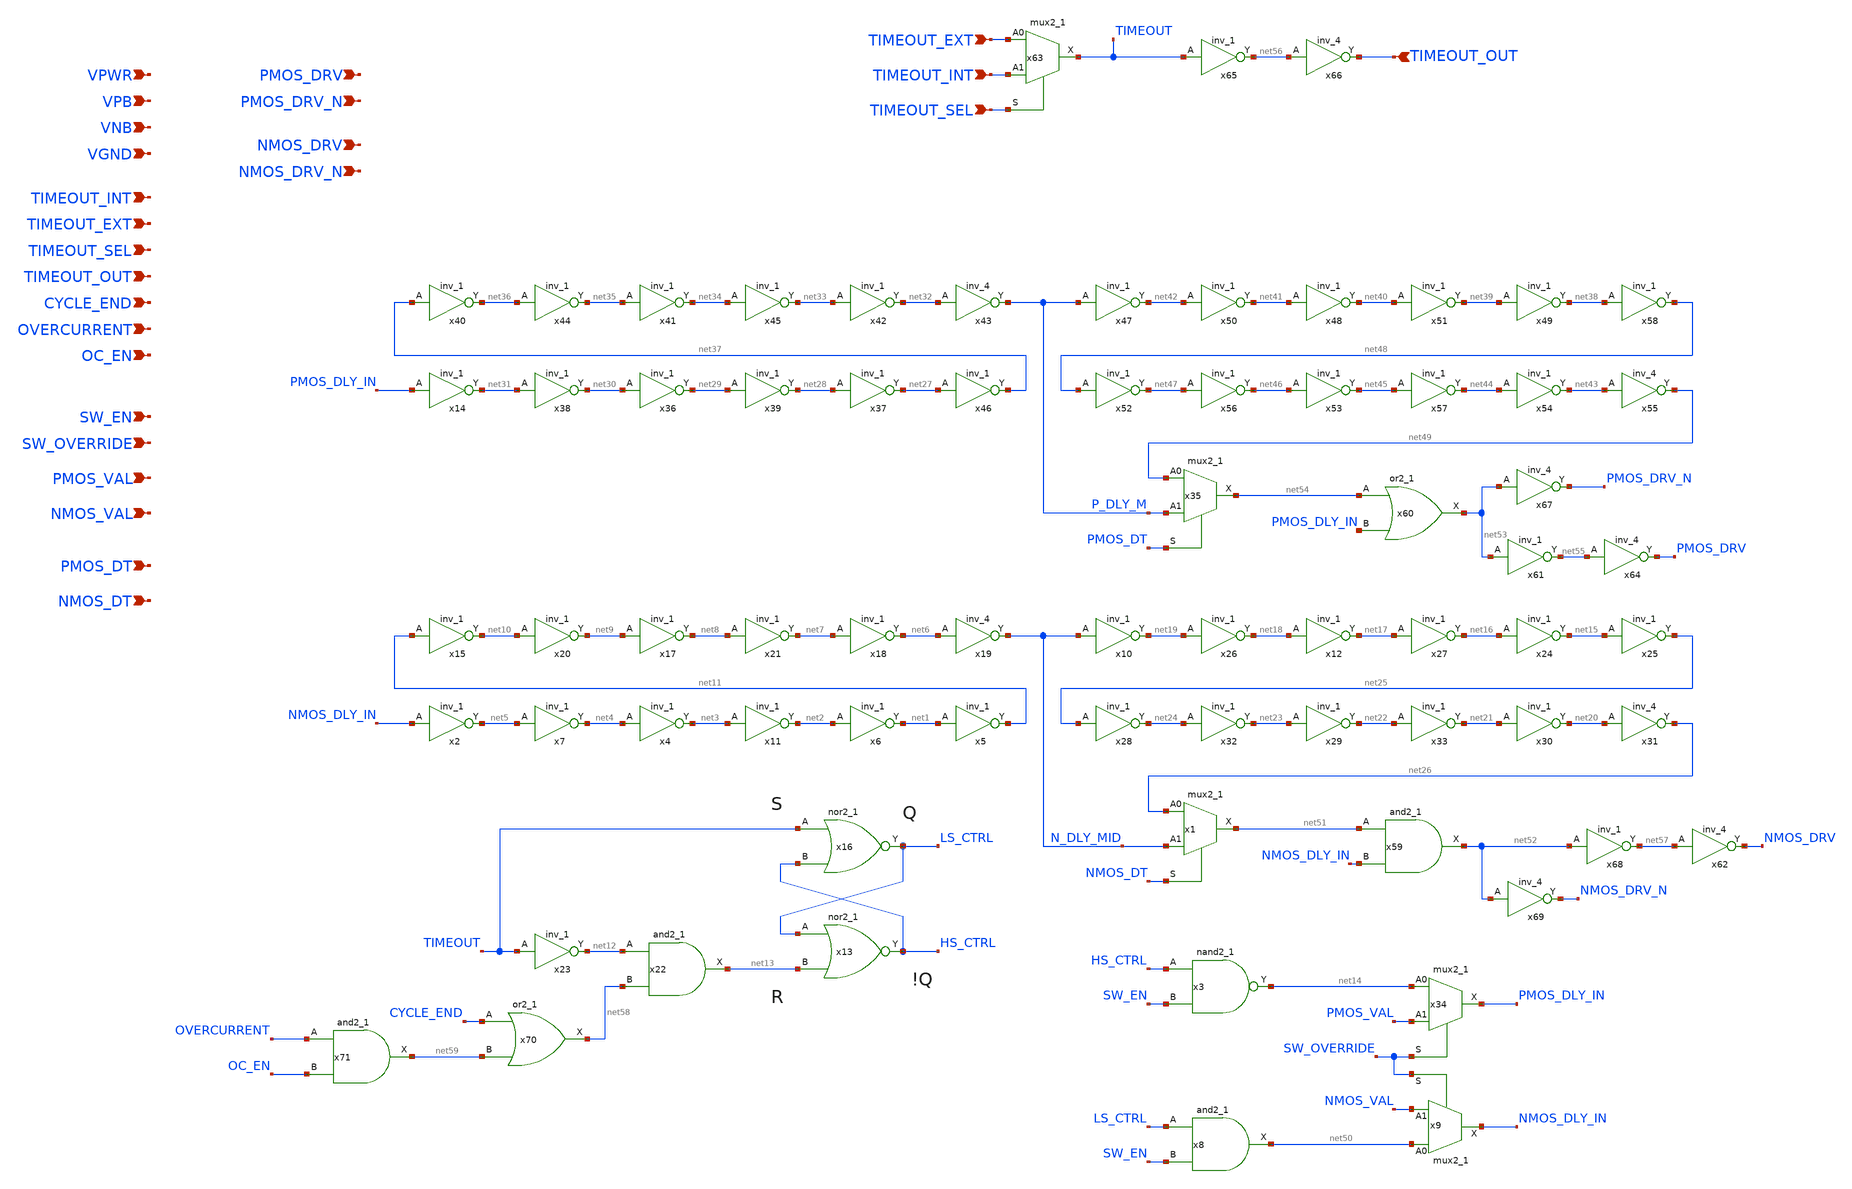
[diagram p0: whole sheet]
** sch_path: design/switch-control/switch_control.sch
**.subckt switch_control VPWR VPB VNB VGND TIMEOUT_INT CYCLE_END SW_EN SW_OVERRIDE PMOS_VAL NMOS_VAL
*+ PMOS_DRV NMOS_DRV PMOS_DT NMOS_DT PMOS_DRV_N NMOS_DRV_N TIMEOUT_EXT TIMEOUT_SEL TIMEOUT_OUT TIMEOUT_SEL
*+ TIMEOUT_INT TIMEOUT_EXT TIMEOUT_OUT OVERCURRENT OC_EN
*.ipin VPWR
*.ipin VPB
*.ipin VNB
*.ipin VGND
*.ipin TIMEOUT_INT
*.ipin CYCLE_END
*.ipin SW_EN
*.ipin SW_OVERRIDE
*.ipin PMOS_VAL
*.ipin NMOS_VAL
*.ipin PMOS_DRV
*.ipin NMOS_DRV
*.ipin PMOS_DT
*.ipin NMOS_DT
*.ipin PMOS_DRV_N
*.ipin NMOS_DRV_N
*.ipin TIMEOUT_EXT
*.ipin TIMEOUT_SEL
*.ipin TIMEOUT_OUT
*.ipin TIMEOUT_SEL
*.ipin TIMEOUT_INT
*.ipin TIMEOUT_EXT
*.ipin TIMEOUT_OUT
*.ipin OVERCURRENT
*.ipin OC_EN
x2 NMOS_DLY_IN VGND VNB VPB VPWR net5 sky130_fd_sc_hvl__inv_1
x1 net26 N_DLY_MID NMOS_DT VGND VNB VPB VPWR net51 sky130_fd_sc_hvl__mux2_1
x4 net4 VGND VNB VPB VPWR net3 sky130_fd_sc_hvl__inv_1
x6 net2 VGND VNB VPB VPWR net1 sky130_fd_sc_hvl__inv_1
x7 net5 VGND VNB VPB VPWR net4 sky130_fd_sc_hvl__inv_1
x11 net3 VGND VNB VPB VPWR net2 sky130_fd_sc_hvl__inv_1
x15 net11 VGND VNB VPB VPWR net10 sky130_fd_sc_hvl__inv_1
x17 net9 VGND VNB VPB VPWR net8 sky130_fd_sc_hvl__inv_1
x18 net7 VGND VNB VPB VPWR net6 sky130_fd_sc_hvl__inv_1
x19 net6 VGND VNB VPB VPWR N_DLY_MID sky130_fd_sc_hvl__inv_4
x20 net10 VGND VNB VPB VPWR net9 sky130_fd_sc_hvl__inv_1
x21 net8 VGND VNB VPB VPWR net7 sky130_fd_sc_hvl__inv_1
x5 net1 VGND VNB VPB VPWR net11 sky130_fd_sc_hvl__inv_1
x22 net12 net58 VGND VNB VPB VPWR net13 sky130_fd_sc_hvl__and2_1
x23 TIMEOUT VGND VNB VPB VPWR net12 sky130_fd_sc_hvl__inv_1
x8 LS_CTRL SW_EN VGND VNB VPB VPWR net50 sky130_fd_sc_hvl__and2_1
x10 N_DLY_MID VGND VNB VPB VPWR net19 sky130_fd_sc_hvl__inv_1
x12 net18 VGND VNB VPB VPWR net17 sky130_fd_sc_hvl__inv_1
x24 net16 VGND VNB VPB VPWR net15 sky130_fd_sc_hvl__inv_1
x26 net19 VGND VNB VPB VPWR net18 sky130_fd_sc_hvl__inv_1
x27 net17 VGND VNB VPB VPWR net16 sky130_fd_sc_hvl__inv_1
x28 net25 VGND VNB VPB VPWR net24 sky130_fd_sc_hvl__inv_1
x29 net23 VGND VNB VPB VPWR net22 sky130_fd_sc_hvl__inv_1
x30 net21 VGND VNB VPB VPWR net20 sky130_fd_sc_hvl__inv_1
x31 net20 VGND VNB VPB VPWR net26 sky130_fd_sc_hvl__inv_4
x32 net24 VGND VNB VPB VPWR net23 sky130_fd_sc_hvl__inv_1
x33 net22 VGND VNB VPB VPWR net21 sky130_fd_sc_hvl__inv_1
x34 net14 PMOS_VAL SW_OVERRIDE VGND VNB VPB VPWR PMOS_DLY_IN sky130_fd_sc_hvl__mux2_1
x25 net15 VGND VNB VPB VPWR net25 sky130_fd_sc_hvl__inv_1
x14 PMOS_DLY_IN VGND VNB VPB VPWR net31 sky130_fd_sc_hvl__inv_1
x35 net49 P_DLY_M PMOS_DT VGND VNB VPB VPWR net54 sky130_fd_sc_hvl__mux2_1
x36 net30 VGND VNB VPB VPWR net29 sky130_fd_sc_hvl__inv_1
x37 net28 VGND VNB VPB VPWR net27 sky130_fd_sc_hvl__inv_1
x38 net31 VGND VNB VPB VPWR net30 sky130_fd_sc_hvl__inv_1
x39 net29 VGND VNB VPB VPWR net28 sky130_fd_sc_hvl__inv_1
x40 net37 VGND VNB VPB VPWR net36 sky130_fd_sc_hvl__inv_1
x41 net35 VGND VNB VPB VPWR net34 sky130_fd_sc_hvl__inv_1
x42 net33 VGND VNB VPB VPWR net32 sky130_fd_sc_hvl__inv_1
x43 net32 VGND VNB VPB VPWR P_DLY_M sky130_fd_sc_hvl__inv_4
x44 net36 VGND VNB VPB VPWR net35 sky130_fd_sc_hvl__inv_1
x45 net34 VGND VNB VPB VPWR net33 sky130_fd_sc_hvl__inv_1
x46 net27 VGND VNB VPB VPWR net37 sky130_fd_sc_hvl__inv_1
x47 P_DLY_M VGND VNB VPB VPWR net42 sky130_fd_sc_hvl__inv_1
x48 net41 VGND VNB VPB VPWR net40 sky130_fd_sc_hvl__inv_1
x49 net39 VGND VNB VPB VPWR net38 sky130_fd_sc_hvl__inv_1
x50 net42 VGND VNB VPB VPWR net41 sky130_fd_sc_hvl__inv_1
x51 net40 VGND VNB VPB VPWR net39 sky130_fd_sc_hvl__inv_1
x52 net48 VGND VNB VPB VPWR net47 sky130_fd_sc_hvl__inv_1
x53 net46 VGND VNB VPB VPWR net45 sky130_fd_sc_hvl__inv_1
x54 net44 VGND VNB VPB VPWR net43 sky130_fd_sc_hvl__inv_1
x55 net43 VGND VNB VPB VPWR net49 sky130_fd_sc_hvl__inv_4
x56 net47 VGND VNB VPB VPWR net46 sky130_fd_sc_hvl__inv_1
x57 net45 VGND VNB VPB VPWR net44 sky130_fd_sc_hvl__inv_1
x58 net38 VGND VNB VPB VPWR net48 sky130_fd_sc_hvl__inv_1
x3 HS_CTRL SW_EN VGND VNB VPB VPWR net14 sky130_fd_sc_hvl__nand2_1
x9 net50 NMOS_VAL SW_OVERRIDE VGND VNB VPB VPWR NMOS_DLY_IN sky130_fd_sc_hvl__mux2_1
x13 LS_CTRL net13 VGND VNB VPB VPWR HS_CTRL sky130_fd_sc_hvl__nor2_1
x16 TIMEOUT HS_CTRL VGND VNB VPB VPWR LS_CTRL sky130_fd_sc_hvl__nor2_1
x59 net51 NMOS_DLY_IN VGND VNB VPB VPWR net52 sky130_fd_sc_hvl__and2_1
x60 net54 PMOS_DLY_IN VGND VNB VPB VPWR net53 sky130_fd_sc_hvl__or2_1
x61 net53 VGND VNB VPB VPWR net55 sky130_fd_sc_hvl__inv_1
x63 TIMEOUT_EXT TIMEOUT_INT TIMEOUT_SEL VGND VNB VPB VPWR TIMEOUT sky130_fd_sc_hvl__mux2_1
x64 net55 VGND VNB VPB VPWR PMOS_DRV sky130_fd_sc_hvl__inv_4
x65 TIMEOUT VGND VNB VPB VPWR net56 sky130_fd_sc_hvl__inv_1
x66 net56 VGND VNB VPB VPWR TIMEOUT_OUT sky130_fd_sc_hvl__inv_4
x67 net53 VGND VNB VPB VPWR PMOS_DRV_N sky130_fd_sc_hvl__inv_4
x68 net52 VGND VNB VPB VPWR net57 sky130_fd_sc_hvl__inv_1
x69 net52 VGND VNB VPB VPWR NMOS_DRV_N sky130_fd_sc_hvl__inv_4
x62 net57 VGND VNB VPB VPWR NMOS_DRV sky130_fd_sc_hvl__inv_4
x70 CYCLE_END net59 VGND VNB VPB VPWR net58 sky130_fd_sc_hvl__or2_1
x71 OVERCURRENT OC_EN VGND VNB VPB VPWR net59 sky130_fd_sc_hvl__and2_1
**.ends
.end
